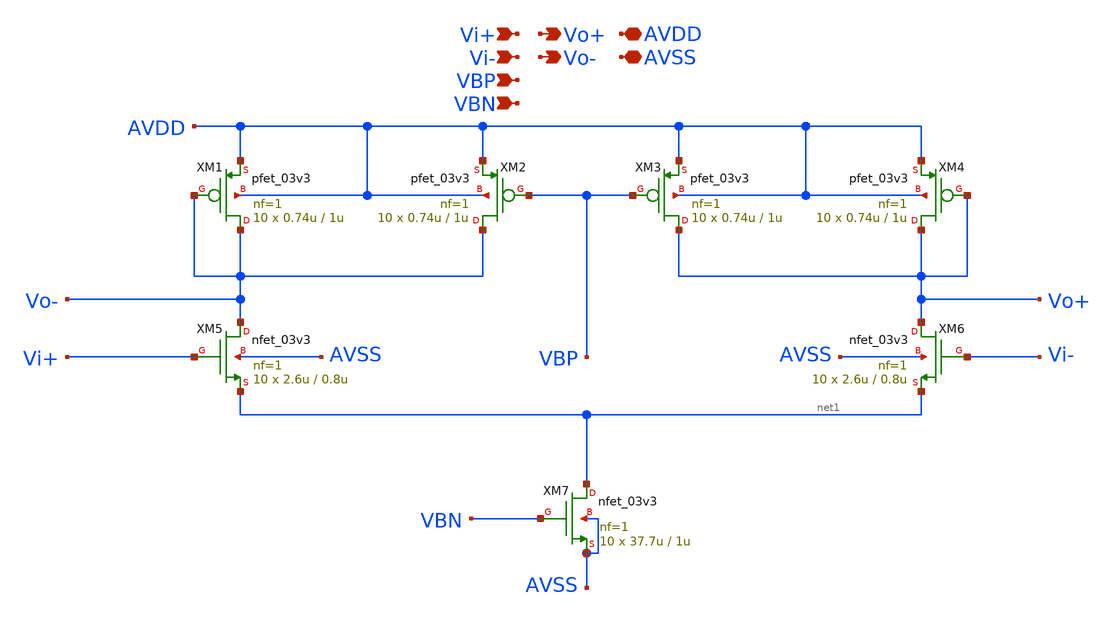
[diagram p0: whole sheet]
** sch_path: designs/libs/core_analog/delay_stage/delay_stage.sch
**.subckt delay_stage Vi+ Vi- Vo+ Vo- AVDD AVSS VBP VBN
*.ipin Vi+
*.ipin Vi-
*.opin Vo+
*.opin Vo-
*.iopin AVDD
*.iopin AVSS
*.ipin VBP
*.ipin VBN
XM5 Vo- Vi+ net1 AVSS nfet_03v3 L=0.8u W=2.6u nf=1 ad='int((nf+1)/2) * W/nf * 0.18u' as='int((nf+2)/2) * W/nf * 0.18u'
+ pd='2*int((nf+1)/2) * (W/nf + 0.18u)' ps='2*int((nf+2)/2) * (W/nf + 0.18u)' nrd='0.18u / W' nrs='0.18u / W'
+ sa=0 sb=0 sd=0 m=10
XM7 net1 VBN AVSS AVSS nfet_03v3 L=1u W=37.7u nf=1 ad='int((nf+1)/2) * W/nf * 0.18u' as='int((nf+2)/2) * W/nf * 0.18u'
+ pd='2*int((nf+1)/2) * (W/nf + 0.18u)' ps='2*int((nf+2)/2) * (W/nf + 0.18u)' nrd='0.18u / W' nrs='0.18u / W'
+ sa=0 sb=0 sd=0 m=10
XM1 Vo- Vo- AVDD AVDD pfet_03v3 L=1u W=0.74u nf=1 ad='int((nf+1)/2) * W/nf * 0.18u' as='int((nf+2)/2) * W/nf * 0.18u'
+ pd='2*int((nf+1)/2) * (W/nf + 0.18u)' ps='2*int((nf+2)/2) * (W/nf + 0.18u)' nrd='0.18u / W' nrs='0.18u / W'
+ sa=0 sb=0 sd=0 m=10
XM6 Vo+ Vi- net1 AVSS nfet_03v3 L=0.8u W=2.6u nf=1 ad='int((nf+1)/2) * W/nf * 0.18u' as='int((nf+2)/2) * W/nf * 0.18u'
+ pd='2*int((nf+1)/2) * (W/nf + 0.18u)' ps='2*int((nf+2)/2) * (W/nf + 0.18u)' nrd='0.18u / W' nrs='0.18u / W'
+ sa=0 sb=0 sd=0 m=10
XM2 Vo- VBP AVDD AVDD pfet_03v3 L=1u W=0.74u nf=1 ad='int((nf+1)/2) * W/nf * 0.18u' as='int((nf+2)/2) * W/nf * 0.18u'
+ pd='2*int((nf+1)/2) * (W/nf + 0.18u)' ps='2*int((nf+2)/2) * (W/nf + 0.18u)' nrd='0.18u / W' nrs='0.18u / W'
+ sa=0 sb=0 sd=0 m=10
XM3 Vo+ VBP AVDD AVDD pfet_03v3 L=1u W=0.74u nf=1 ad='int((nf+1)/2) * W/nf * 0.18u' as='int((nf+2)/2) * W/nf * 0.18u'
+ pd='2*int((nf+1)/2) * (W/nf + 0.18u)' ps='2*int((nf+2)/2) * (W/nf + 0.18u)' nrd='0.18u / W' nrs='0.18u / W'
+ sa=0 sb=0 sd=0 m=10
XM4 Vo+ Vo+ AVDD AVDD pfet_03v3 L=1u W=0.74u nf=1 ad='int((nf+1)/2) * W/nf * 0.18u' as='int((nf+2)/2) * W/nf * 0.18u'
+ pd='2*int((nf+1)/2) * (W/nf + 0.18u)' ps='2*int((nf+2)/2) * (W/nf + 0.18u)' nrd='0.18u / W' nrs='0.18u / W'
+ sa=0 sb=0 sd=0 m=10
**.ends
.end
